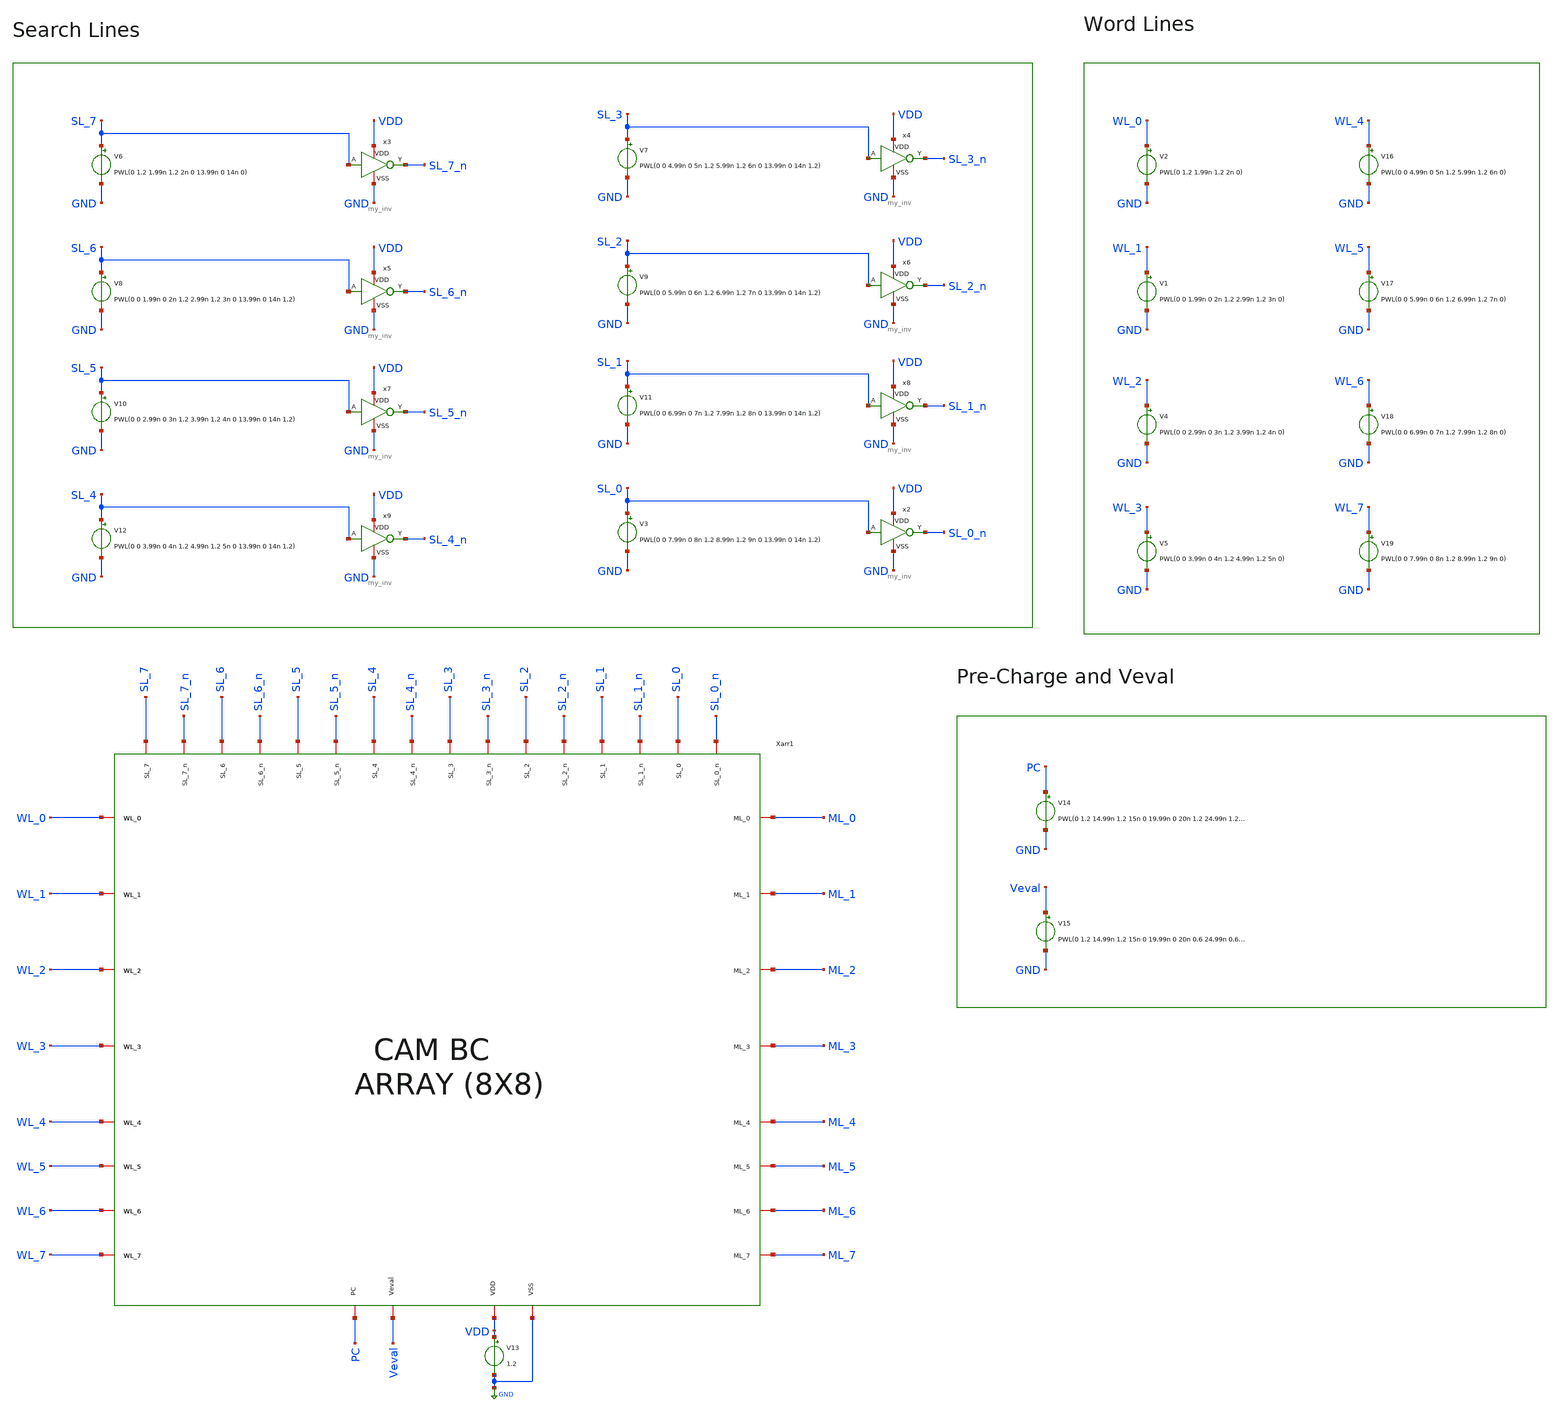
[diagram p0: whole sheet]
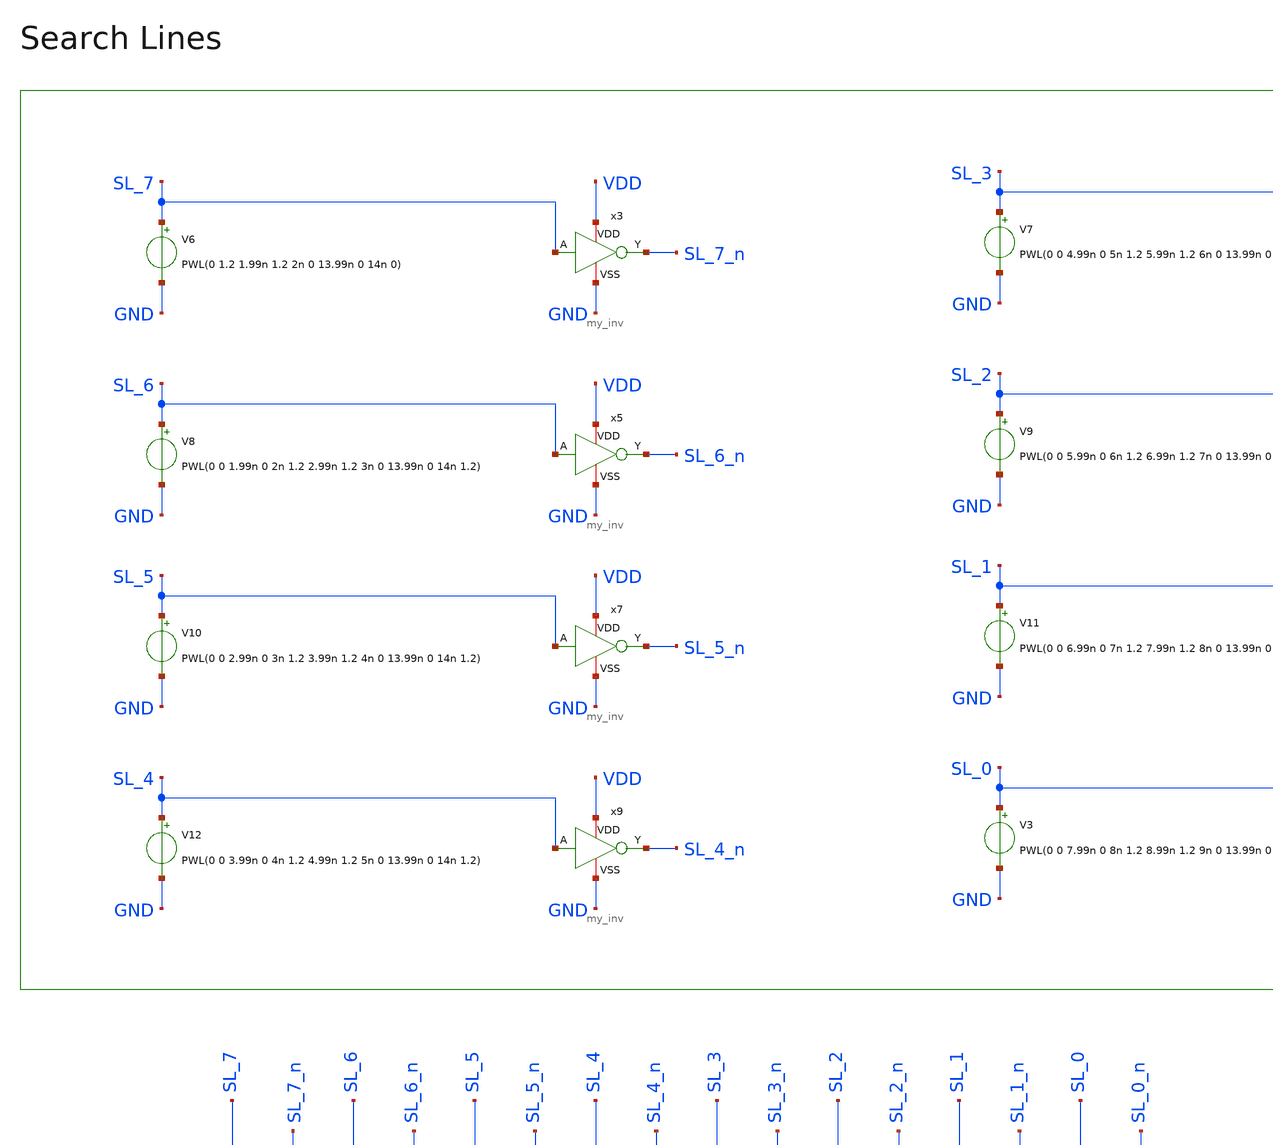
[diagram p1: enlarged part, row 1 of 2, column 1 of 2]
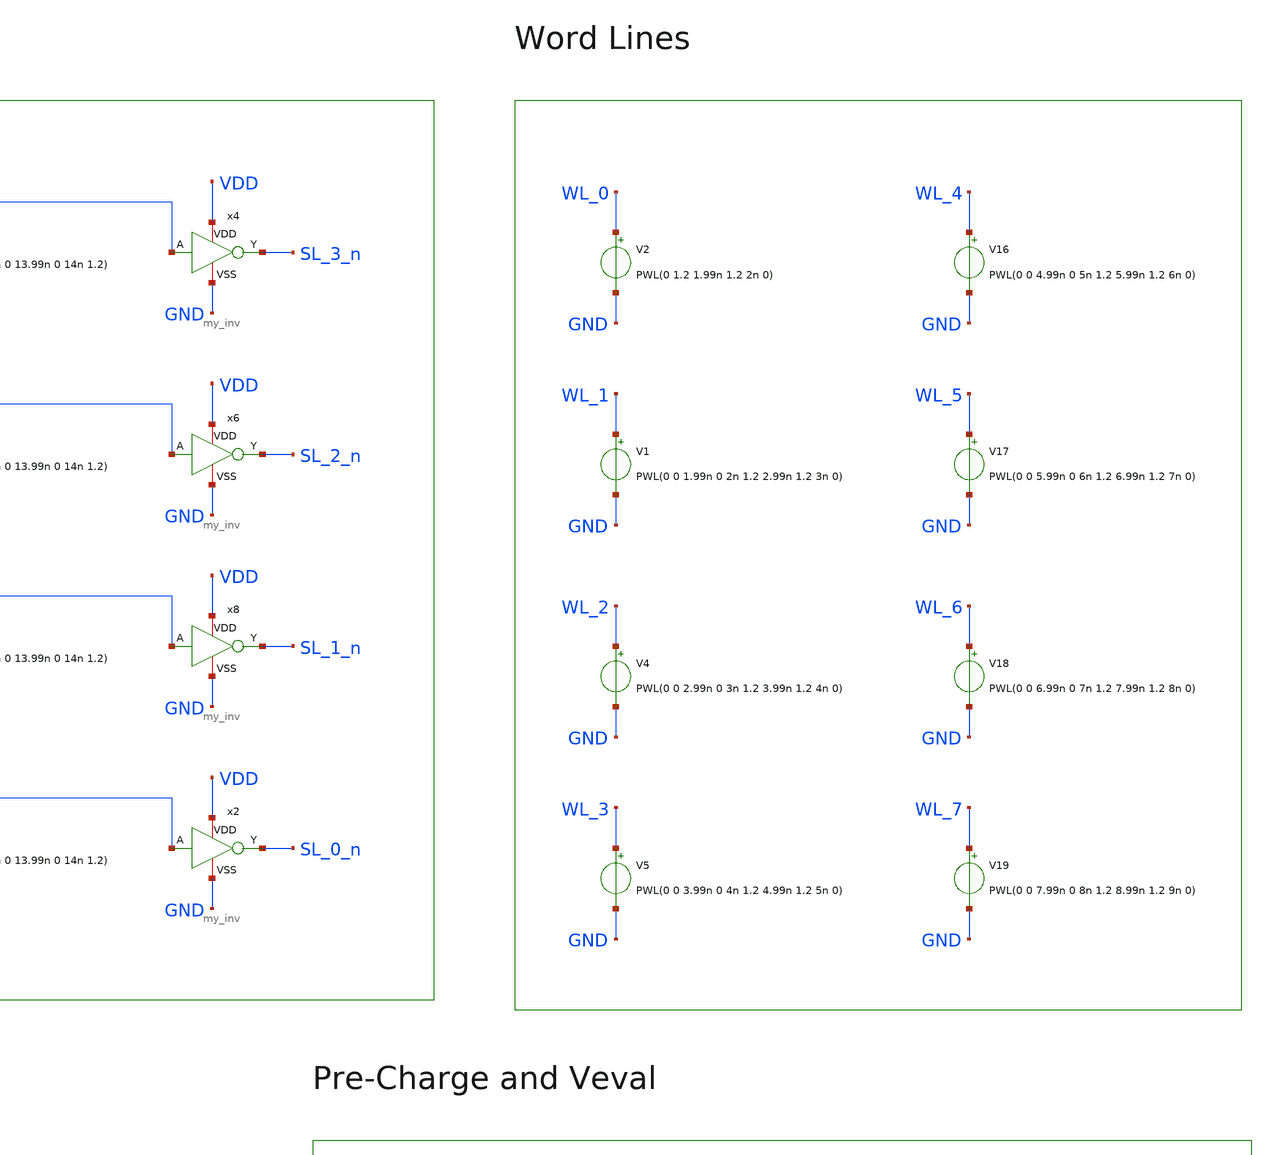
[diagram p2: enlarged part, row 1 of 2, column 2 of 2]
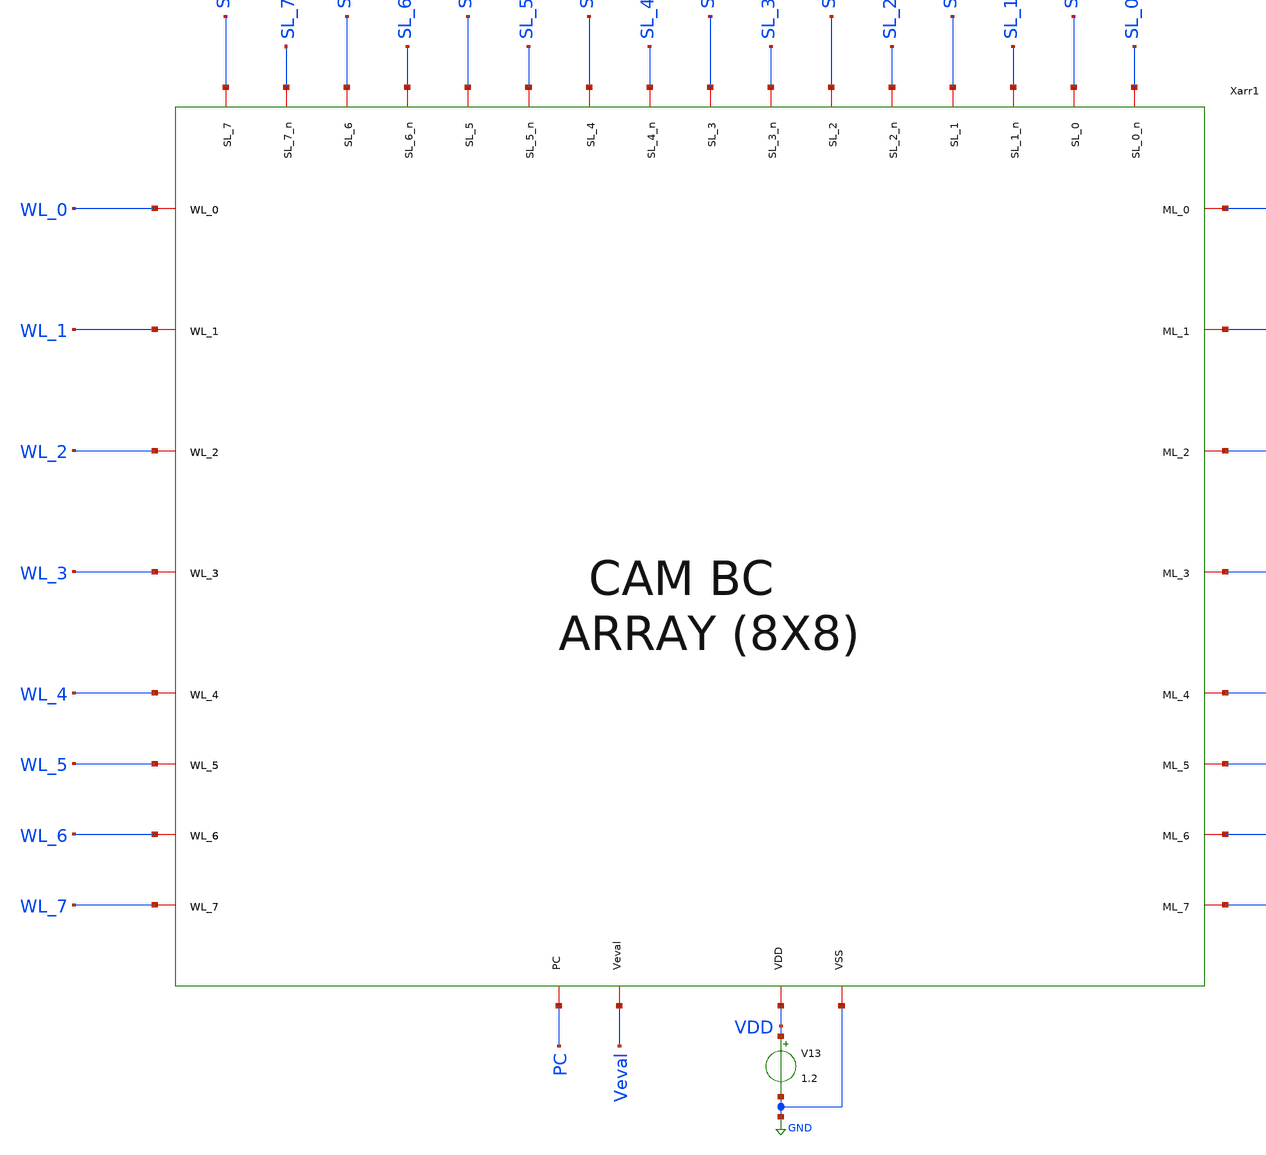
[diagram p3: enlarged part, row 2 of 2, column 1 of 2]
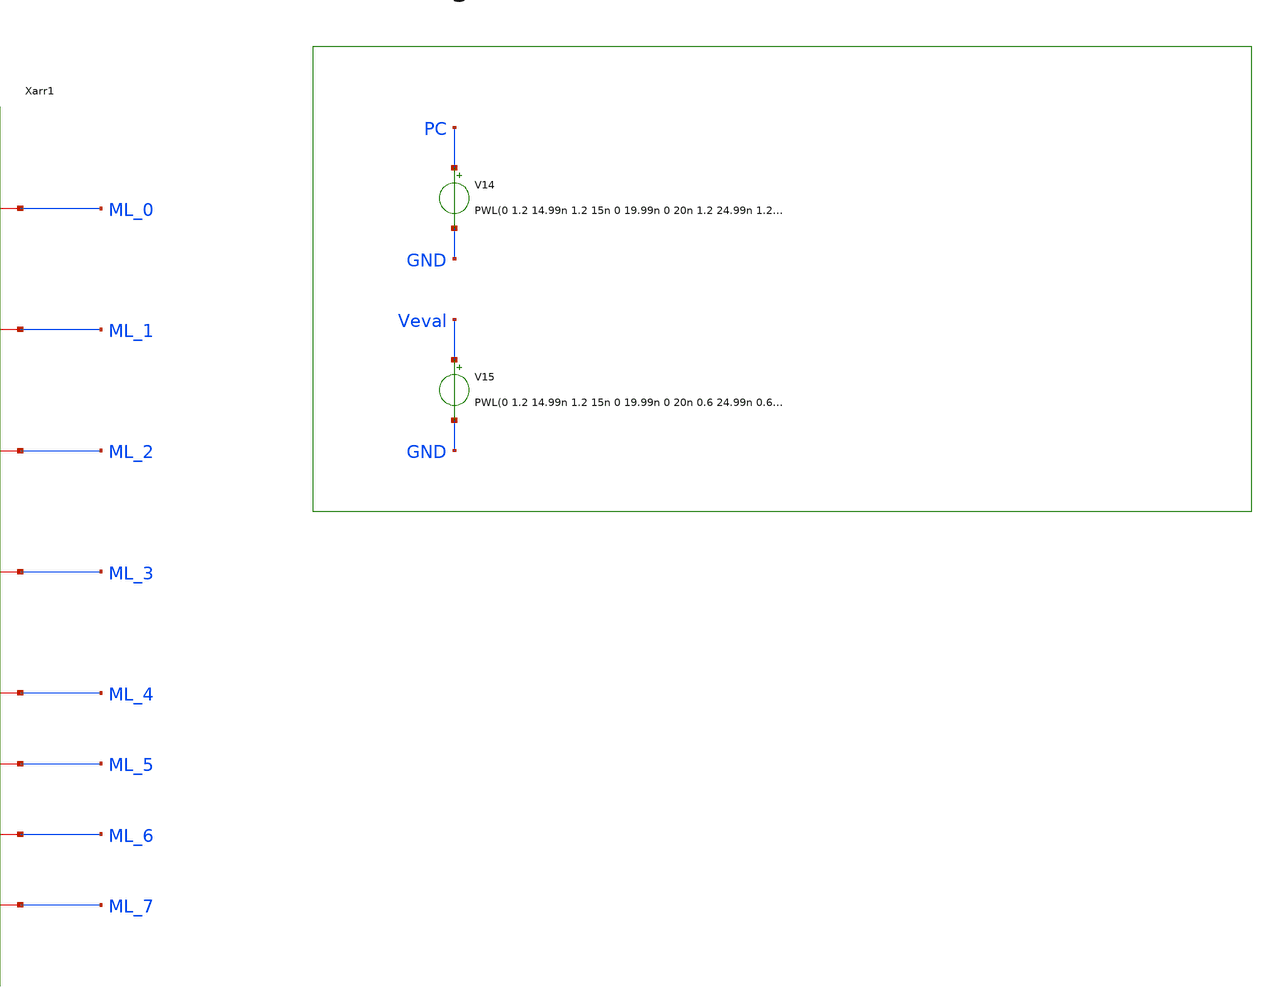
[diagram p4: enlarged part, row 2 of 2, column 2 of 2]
** sch_path: xschem/array_8x8_TB.sch
**.subckt array_8x8_TB
Xarr1 SL_6_n SL_4_n SL_0_n SL_3 SL_2 SL_2_n SL_0 ML_0 SL_7 SL_5_n SL_5 SL_3_n SL_1 SL_1_n SL_6 WL_0
+ SL_4 SL_7_n VDD GND Veval PC ML_1 WL_1 WL_2 ML_2 WL_3 ML_3 ML_4 WL_4 ML_5 WL_5 ML_6 WL_6 ML_7 WL_7
+ array_8x8
V3 SL_0 GND PWL(0 0 7.99n 0 8n 1.2 8.99n 1.2 9n 0 13.99n 0 14n 1.2)
x2 VDD SL_0_n SL_0 GND my_inv
V6 SL_7 GND PWL(0 1.2 1.99n 1.2 2n 0 13.99n 0 14n 0)
x3 VDD SL_7_n SL_7 GND my_inv
V7 SL_3 GND PWL(0 0 4.99n 0 5n 1.2 5.99n 1.2 6n 0 13.99n 0 14n 1.2)
x4 VDD SL_3_n SL_3 GND my_inv
V8 SL_6 GND PWL(0 0 1.99n 0 2n 1.2 2.99n 1.2 3n 0 13.99n 0 14n 1.2)
x5 VDD SL_6_n SL_6 GND my_inv
V9 SL_2 GND PWL(0 0 5.99n 0 6n 1.2 6.99n 1.2 7n 0 13.99n 0 14n 1.2)
x6 VDD SL_2_n SL_2 GND my_inv
V10 SL_5 GND PWL(0 0 2.99n 0 3n 1.2 3.99n 1.2 4n 0 13.99n 0 14n 1.2)
x7 VDD SL_5_n SL_5 GND my_inv
V11 SL_1 GND PWL(0 0 6.99n 0 7n 1.2 7.99n 1.2 8n 0 13.99n 0 14n 1.2)
x8 VDD SL_1_n SL_1 GND my_inv
V12 SL_4 GND PWL(0 0 3.99n 0 4n 1.2 4.99n 1.2 5n 0 13.99n 0 14n 1.2)
x9 VDD SL_4_n SL_4 GND my_inv
V13 VDD GND 1.2
V14 PC GND PWL(0 1.2 14.99n 1.2 15n 0 19.99n 0 20n 1.2 24.99n 1.2 25n 0 29.99n 0 30n 1.2 34.99n 1.2
+ 35n 0 39.99n 0 40n 1.2)
V15 Veval GND PWL(0 1.2 14.99n 1.2 15n 0 19.99n 0 20n 0.6 24.99n 0.6 25n 0 29.99n 0 30n 0.55 34.99n
+ 0.55 35n 0 39.99n 0 40n 0.5)
V2 WL_0 GND PWL(0 1.2 1.99n 1.2 2n 0)
V1 WL_1 GND PWL(0 0 1.99n 0 2n 1.2 2.99n 1.2 3n 0)
V4 WL_2 GND PWL(0 0 2.99n 0 3n 1.2 3.99n 1.2 4n 0)
V5 WL_3 GND PWL(0 0 3.99n 0 4n 1.2 4.99n 1.2 5n 0)
V16 WL_4 GND PWL(0 0 4.99n 0 5n 1.2 5.99n 1.2 6n 0)
V17 WL_5 GND PWL(0 0 5.99n 0 6n 1.2 6.99n 1.2 7n 0)
V18 WL_6 GND PWL(0 0 6.99n 0 7n 1.2 7.99n 1.2 8n 0)
V19 WL_7 GND PWL(0 0 7.99n 0 8n 1.2 8.99n 1.2 9n 0)
**** begin user architecture code



.lib cornerMOSlv.lib mos_tt
.lib cornerMOShv.lib mos_tt
.lib cornerHBT.lib hbt_typ
.lib cornerRES.lib res_typ
.lib cornerCAP.lib cap_typ
.tran 1n 50n
.save time v(ML_0) v(ML_1) v(ML_2) v(ML_3) v(ML_4) v(ML_5) v(ML_6) v(ML_7) v(PC) v(Veval) v(WL_0) v(WL_1) v(WL_2) v(WL_3) v(WL_4) v(WL_5) v(WL_6) v(WL_7)
.control
set wr_vecnames
run
wrdata /home/designer/shared/tran_data.txt v(ML_0) v(ML_1) v(ML_2) v(ML_3) v(ML_4) v(ML_5) v(ML_6)
+ v(ML_7) v(WL_0) v(WL_1) v(WL_2) v(WL_3) v(WL_4) v(WL_5) v(WL_6) v(WL_7) v(PC) v(Veval)
quit
.endc



**** end user architecture code
**.ends

* expanding   symbol:  array_8x8.sym # of pins=44
** sym_path: xschem/array_8x8.sym
** sch_path: xschem/array_8x8.sch
.subckt array_8x8 SL_6_n SL_4_n SL_0_n SL_3 SL_2 SL_2_n SL_0 ML_0 SL_7 SL_5_n SL_5 SL_3_n SL_1
+ SL_1_n SL_6 WL_0 SL_4 SL_7_n VDD VSS Veval PC ML_1 WL_1 WL_2 ML_2 WL_3 ML_3 ML_4 WL_4 ML_5 WL_5 ML_6 WL_6
+ ML_7 WL_7
*.iopin WL_0
*.iopin ML_0
*.iopin VDD
*.iopin VSS
*.iopin Veval
*.iopin PC
*.iopin WL_1
*.iopin ML_1
*.iopin WL_2
*.iopin ML_2
*.iopin WL_3
*.iopin ML_3
*.iopin WL_4
*.iopin ML_4
*.iopin WL_5
*.iopin ML_5
*.iopin WL_6
*.iopin ML_6
*.iopin WL_7
*.iopin ML_7
*.iopin SL_7
*.iopin SL_7_n
*.iopin SL_6
*.iopin SL_5
*.iopin SL_4
*.iopin SL_3
*.iopin SL_2
*.iopin SL_1
*.iopin SL_0
*.iopin SL_6_n
*.iopin SL_5_n
*.iopin SL_4_n
*.iopin SL_3_n
*.iopin SL_2_n
*.iopin SL_1_n
*.iopin SL_0_n
Xwc81 SL_3_n SL_1_n SL_2_n SL_0_n SL_7 SL_6 SL_5 SL_4 SL_3 SL_2 SL_1 SL_0 SL_7_n SL_6_n SL_5_n
+ SL_4_n WL_0 ML_0 VDD Veval VSS PC word_cell_8
Xwc82 SL_3_n SL_1_n SL_2_n SL_0_n SL_7 SL_6 SL_5 SL_4 SL_3 SL_2 SL_1 SL_0 SL_7_n SL_6_n SL_5_n
+ SL_4_n WL_1 ML_1 VDD Veval VSS PC word_cell_8
Xwc83 SL_3_n SL_1_n SL_2_n SL_0_n SL_7 SL_6 SL_5 SL_4 SL_3 SL_2 SL_1 SL_0 SL_7_n SL_6_n SL_5_n
+ SL_4_n WL_2 ML_2 VDD Veval VSS PC word_cell_8
Xwc84 SL_3_n SL_1_n SL_2_n SL_0_n SL_7 SL_6 SL_5 SL_4 SL_3 SL_2 SL_1 SL_0 SL_7_n SL_6_n SL_5_n
+ SL_4_n WL_3 ML_3 VDD Veval VSS PC word_cell_8
Xwc85 SL_3_n SL_1_n SL_2_n SL_0_n SL_7 SL_6 SL_5 SL_4 SL_3 SL_2 SL_1 SL_0 SL_7_n SL_6_n SL_5_n
+ SL_4_n WL_4 ML_4 VDD Veval VSS PC word_cell_8
Xwc86 SL_3_n SL_1_n SL_2_n SL_0_n SL_7 SL_6 SL_5 SL_4 SL_3 SL_2 SL_1 SL_0 SL_7_n SL_6_n SL_5_n
+ SL_4_n WL_5 ML_5 VDD Veval VSS PC word_cell_8
Xwc87 SL_3_n SL_1_n SL_2_n SL_0_n SL_7 SL_6 SL_5 SL_4 SL_3 SL_2 SL_1 SL_0 SL_7_n SL_6_n SL_5_n
+ SL_4_n WL_6 ML_6 VDD Veval VSS PC word_cell_8
Xwc88 SL_3_n SL_1_n SL_2_n SL_0_n SL_7 SL_6 SL_5 SL_4 SL_3 SL_2 SL_1 SL_0 SL_7_n SL_6_n SL_5_n
+ SL_4_n WL_7 ML_7 VDD Veval VSS PC word_cell_8
.ends


* expanding   symbol:  my_inv.sym # of pins=4
** sym_path: xschem/my_inv.sym
** sch_path: xschem/my_inv.sch
.subckt my_inv VDD Y A VSS
*.opin Y
*.ipin A
*.iopin VDD
*.iopin VSS
XMN0 Y A VSS VSS sg13_lv_nmos w=740.00n l=130.00n ng=1 m=1 mm_ok=1
XMP0 Y A VDD VDD sg13_lv_pmos w=1.12u l=130.00n ng=1 m=1 mm_ok=1
.ends


* expanding   symbol:  /home/designer/shared/word_cell_8.sym # of pins=22
** sym_path: xschem/word_cell_8.sym
** sch_path: xschem/word_cell_8.sch
.subckt word_cell_8 SL_3_n SL_1_n SL_2_n SL_0_n SL_7 SL_6 SL_5 SL_4 SL_3 SL_2 SL_1 SL_0 SL_7_n
+ SL_6_n SL_5_n SL_4_n WL ML VDD Veval VSS PC
*.iopin VSS
*.iopin Veval
*.iopin VDD
*.iopin WL
*.iopin ML
*.iopin SL_7
*.iopin SL_6
*.iopin SL_5
*.iopin SL_4
*.iopin SL_3
*.iopin SL_2
*.iopin SL_1
*.iopin SL_0
*.iopin SL_7_n
*.iopin SL_6_n
*.iopin SL_5_n
*.iopin SL_4_n
*.iopin SL_3_n
*.iopin SL_2_n
*.iopin SL_1_n
*.iopin SL_0_n
*.ipin PC
Xbc1 WL SL_7 SL_7_n VDD ML Veval VSS bitcell
Xbc2 WL SL_6 SL_6_n VDD ML Veval VSS bitcell
Xbc3 WL SL_5 SL_5_n VDD ML Veval VSS bitcell
Xbc4 WL SL_4 SL_4_n VDD ML Veval VSS bitcell
Xbc5 WL SL_3 SL_3_n VDD ML Veval VSS bitcell
Xbc6 WL SL_2 SL_2_n VDD ML Veval VSS bitcell
Xbc7 WL SL_1 SL_1_n VDD ML Veval VSS bitcell
Xbc8 WL SL_0 SL_0_n VDD ML Veval VSS bitcell
XMP0 ML PC VDD VDD sg13_lv_pmos w=2.24u l=130.00n ng=1 m=1 mm_ok=1
.ends


* expanding   symbol:  /home/designer/shared/bitcell.sym # of pins=7
** sym_path: xschem/bitcell.sym
** sch_path: xschem/bitcell.sch
.subckt bitcell WL SL SL_n VDD ML Veval VSS
*.ipin SL
*.ipin SL_n
*.ipin WL
*.iopin ML
*.ipin Veval
*.iopin VDD
*.iopin VSS
XMN1 SL WL D_n VSS sg13_lv_nmos w=740.00n l=130.00n ng=1 m=1 mm_ok=1
XMN2 SL_n WL D VSS sg13_lv_nmos w=740.00n l=130.00n ng=1 m=1 mm_ok=1
XMN3 net1 D_n SL VSS sg13_lv_nmos w=740.00n l=130.00n ng=1 m=1 mm_ok=1
XMN4 net1 D SL_n VSS sg13_lv_nmos w=740.00n l=130.00n ng=1 m=1 mm_ok=1
XMN5 ML net1 net2 VSS sg13_lv_nmos w=740.00n l=130.00n ng=1 m=1 mm_ok=1
XMN6 net2 Veval VSS VSS sg13_lv_nmos w=740.00n l=130.00n ng=1 m=1 mm_ok=1
X1 VDD D D_n VSS my_inv
X2 VDD D_n D VSS my_inv
.ends

.GLOBAL GND
.end
